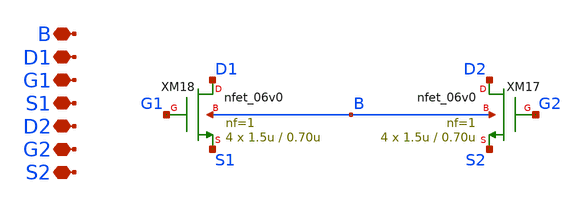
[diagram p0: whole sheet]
** sch_path: designs/libs/core_single-fet/nfet-pin/nfet-pin.sch
**.subckt nfet-pin D1 B G1 S1 D2 G2 S2
*.iopin D1
*.iopin B
*.iopin G1
*.iopin S1
*.iopin D2
*.iopin G2
*.iopin S2
XM17 D2 G2 S2 B nfet_06v0 L=0.70u W=1.5u nf=1 ad='int((nf+1)/2) * W/nf * 0.18u' as='int((nf+2)/2) * W/nf * 0.18u'
+ pd='2*int((nf+1)/2) * (W/nf + 0.18u)' ps='2*int((nf+2)/2) * (W/nf + 0.18u)' nrd='0.18u / W' nrs='0.18u / W'
+ sa=0 sb=0 sd=0 m=4
XM18 D1 G1 S1 B nfet_06v0 L=0.70u W=1.5u nf=1 ad='int((nf+1)/2) * W/nf * 0.18u' as='int((nf+2)/2) * W/nf * 0.18u'
+ pd='2*int((nf+1)/2) * (W/nf + 0.18u)' ps='2*int((nf+2)/2) * (W/nf + 0.18u)' nrd='0.18u / W' nrs='0.18u / W'
+ sa=0 sb=0 sd=0 m=4
**.ends
.end
